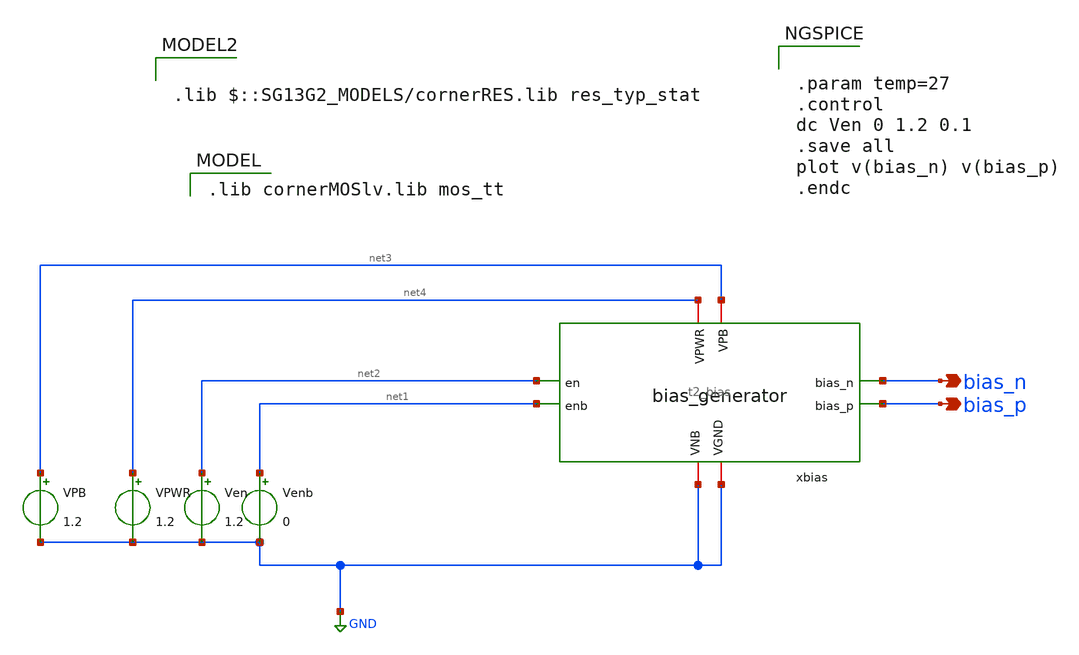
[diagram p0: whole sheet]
** sch_path: Team 2 Design/design_data/xschem/t2_bias_tb.sch
**.subckt t2_bias_tb bias_n bias_p
*.opin bias_n
*.opin bias_p
VPB net3 GND 1.2
Venb net1 GND 0
Ven net2 GND 1.2
VPWR net4 GND 1.2
x1 net4 net3 GND GND net2 bias_n bias_p net1 t2_bias
**** begin user architecture code
 .lib cornerMOSlv.lib mos_tt



.param temp=27
.control
dc Ven 0 1.2 0.1
.save all
plot v(bias_n) v(bias_p)
.endc



.lib $::SG13G2_MODELS/cornerRES.lib res_typ_stat

**** end user architecture code
**.ends

* expanding   symbol:  /foss/designs/cmos-pll-ihp-sg13g2/Team 2
*+ Design/design_data/xschem/t2_bias.sym # of pins=8
** sym_path: Team Designs/Team 2 Design/design_data/xschem/t2_bias.sym
** sch_path: Team Designs/Team 2 Design/design_data/xschem/t2_bias.sch
.subckt t2_bias VPWR VPB VGND VNB en bias_n bias_p enb
*.iopin VPWR
*.iopin VPB
*.iopin VGND
*.iopin VNB
*.ipin en
*.ipin enb
*.opin bias_n
*.opin bias_p
XM9 net1 en VPWR VPB sg13_lv_pmos w=0.5u l=0.15u ng=1 m=1 mm_ok=1
XM10 bias_p bias_p VPWR VPB sg13_lv_pmos w=0.2u l=1.0u ng=1 m=5 mm_ok=1
XM1 dio_mid dio_mid VPWR VPB sg13_lv_pmos w=0.5u l=0.15u ng=1 m=1 mm_ok=1
XM2 net1 net1 dio_mid VPB sg13_lv_pmos w=0.5u l=0.15u ng=1 m=1 mm_ok=1
XM3 bias_p en VPWR VPB sg13_lv_pmos w=0.5u l=0.15u ng=1 m=1 mm_ok=1
XM4 bias_n bias_p res_bot VPB sg13_lv_pmos w=0.2u l=1.0u ng=1 m=5 mm_ok=1
XM11 kick_sw en VGND VNB sg13_lv_nmos w=0.5u l=0.15u ng=1 m=1 mm_ok=1
XM12 bias_p net1 kick_sw VNB sg13_lv_nmos w=0.5u l=0.15u ng=1 m=1 mm_ok=1
XM5 net1 bias_n VGND VNB sg13_lv_nmos w=0.2u l=1.0u ng=1 m=5 mm_ok=1
XM6 bias_p bias_n VGND VNB sg13_lv_nmos w=0.2u l=1.0u ng=1 m=5 mm_ok=1
XM7 bias_n enb VGND VNB sg13_lv_nmos w=0.5u l=0.15u ng=1 m=1 mm_ok=1
XM8 bias_n bias_n VGND VNB sg13_lv_nmos w=0.2u l=1.0u ng=1 m=5 mm_ok=1
XR1 VPWR res_bot sub! rhigh w=0.5e-6 l=0.5e-6 m=1 b=0 mm_ok=1
.ends

.GLOBAL GND
.end
